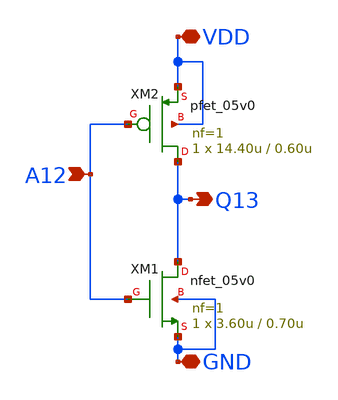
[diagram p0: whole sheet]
** sch_path: member_project/bols-blue/inv.sch
**.subckt inv A12 Q13 VDD GND
*.ipin A12
*.opin Q13
*.iopin VDD
*.iopin GND
XM1 Q13 A12 GND GND nfet_05v0 L=0.70u W=3.60u nf=1 ad='int((nf+1)/2) * W/nf * 0.18u' as='int((nf+2)/2) * W/nf * 0.18u'
+ pd='2*int((nf+1)/2) * (W/nf + 0.18u)' ps='2*int((nf+2)/2) * (W/nf + 0.18u)' nrd='0.18u / W' nrs='0.18u / W'
+ sa=0 sb=0 sd=0 m=1
XM2 Q13 A12 VDD VDD pfet_05v0 L=0.60u W=14.40u nf=1 ad='int((nf+1)/2) * W/nf * 0.18u' as='int((nf+2)/2) * W/nf * 0.18u'
+ pd='2*int((nf+1)/2) * (W/nf + 0.18u)' ps='2*int((nf+2)/2) * (W/nf + 0.18u)' nrd='0.18u / W' nrs='0.18u / W'
+ sa=0 sb=0 sd=0 m=1
**.ends
.end
